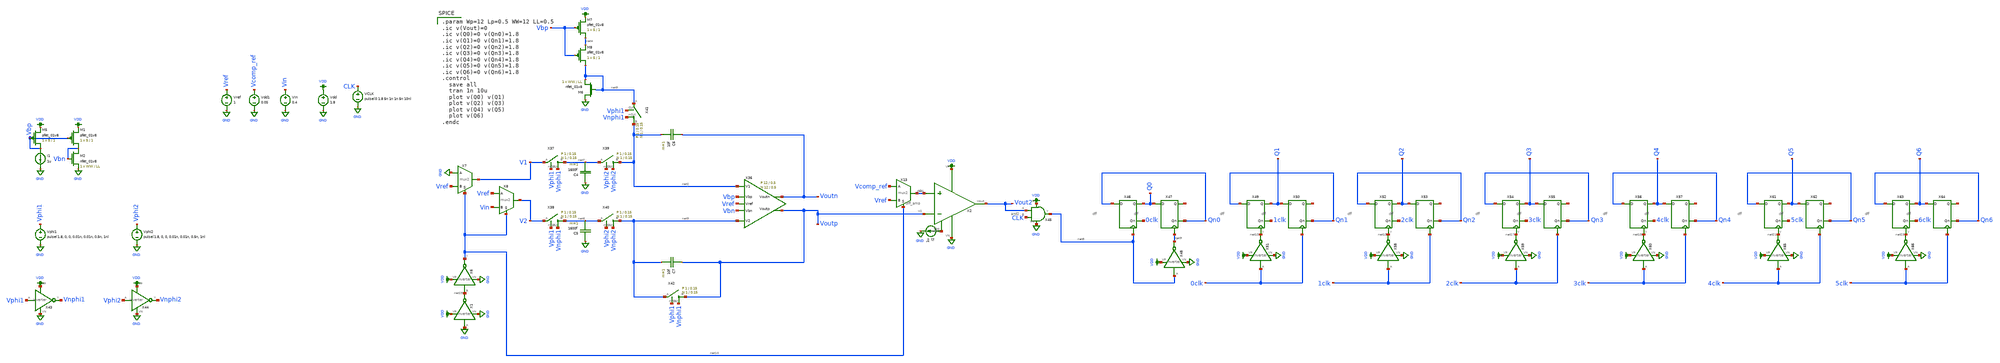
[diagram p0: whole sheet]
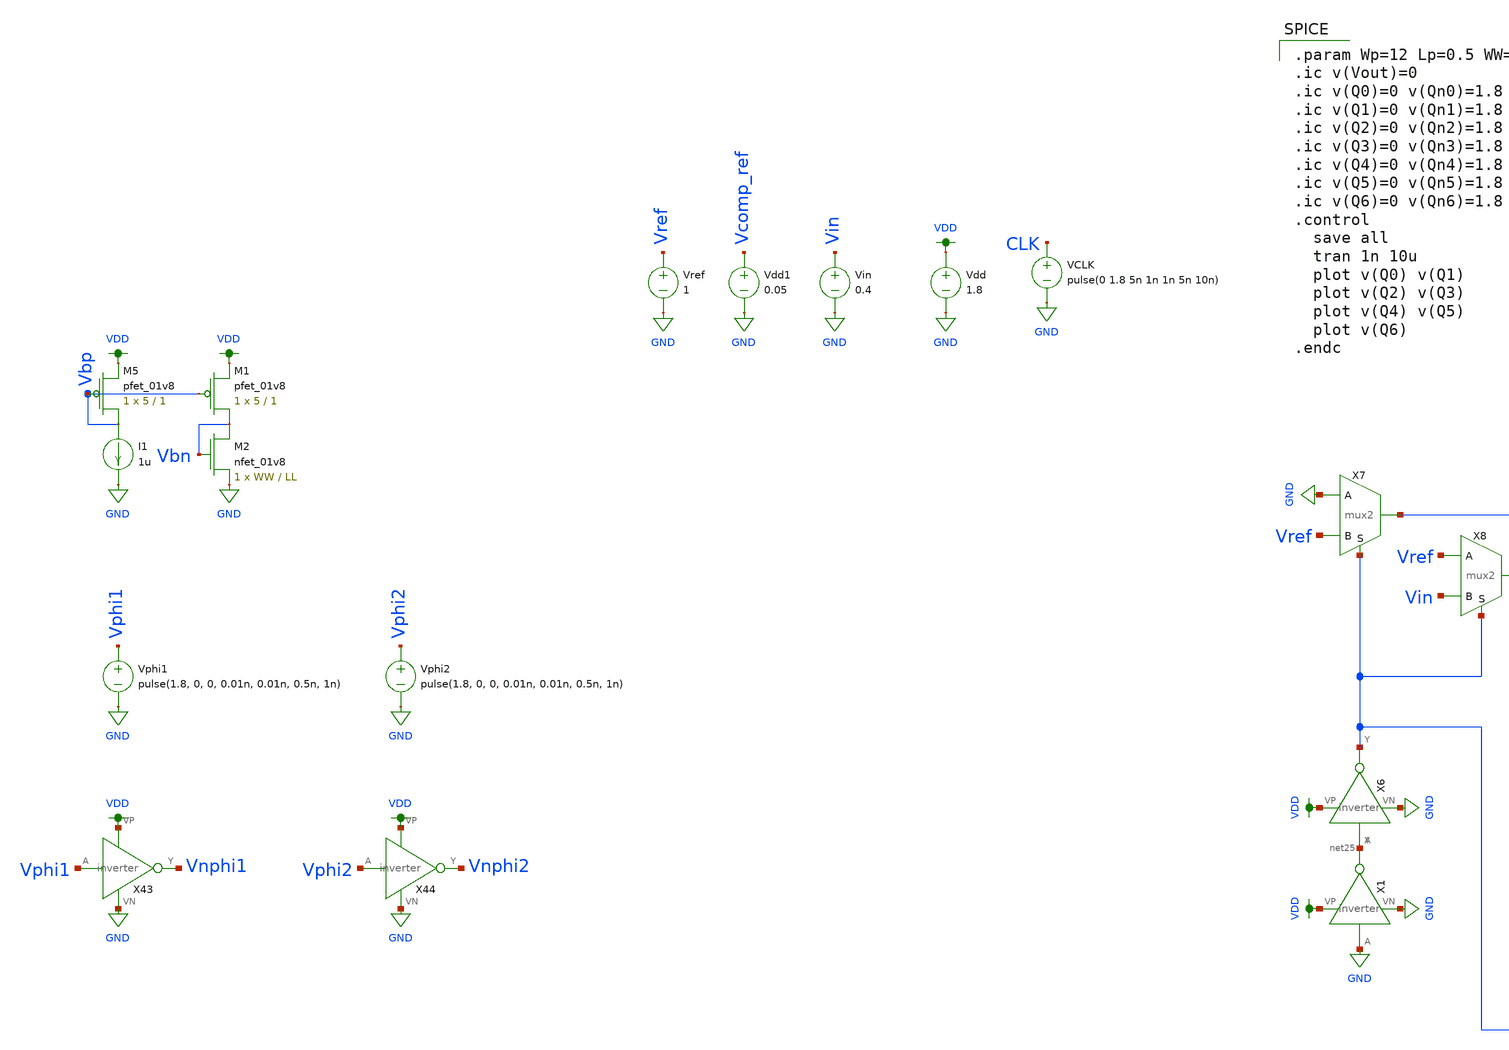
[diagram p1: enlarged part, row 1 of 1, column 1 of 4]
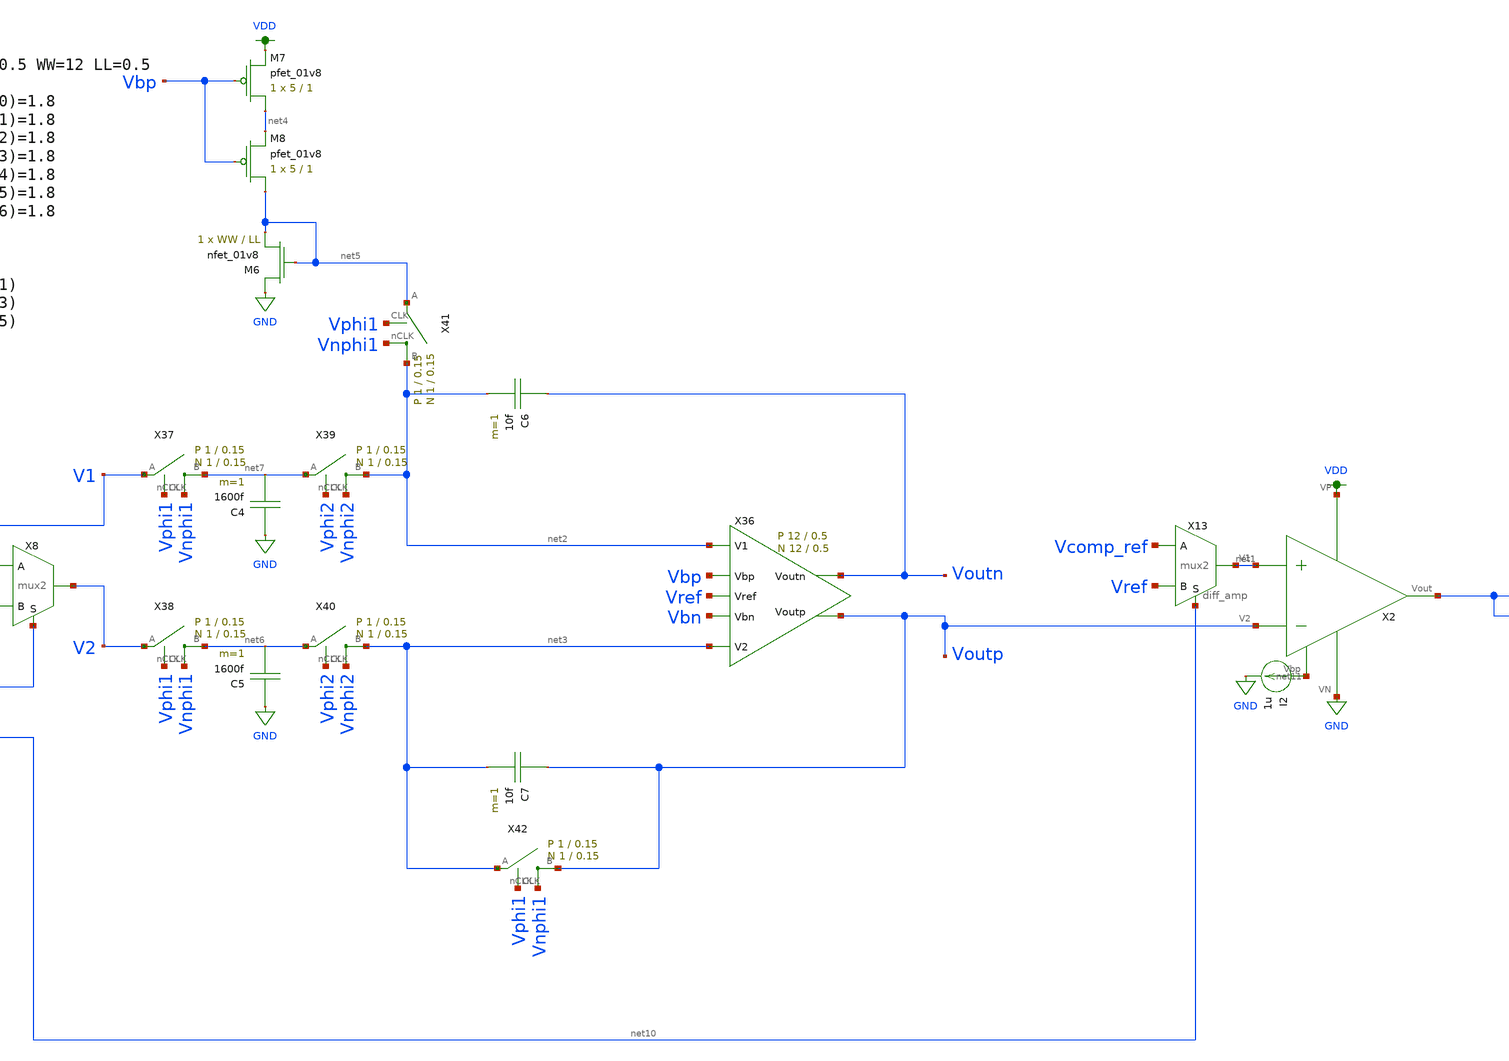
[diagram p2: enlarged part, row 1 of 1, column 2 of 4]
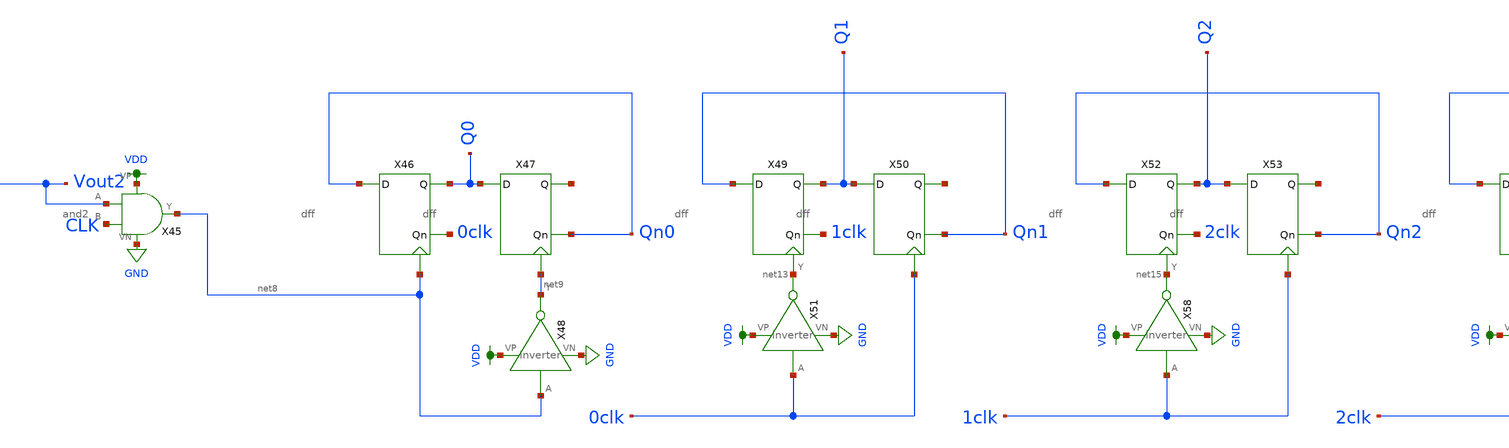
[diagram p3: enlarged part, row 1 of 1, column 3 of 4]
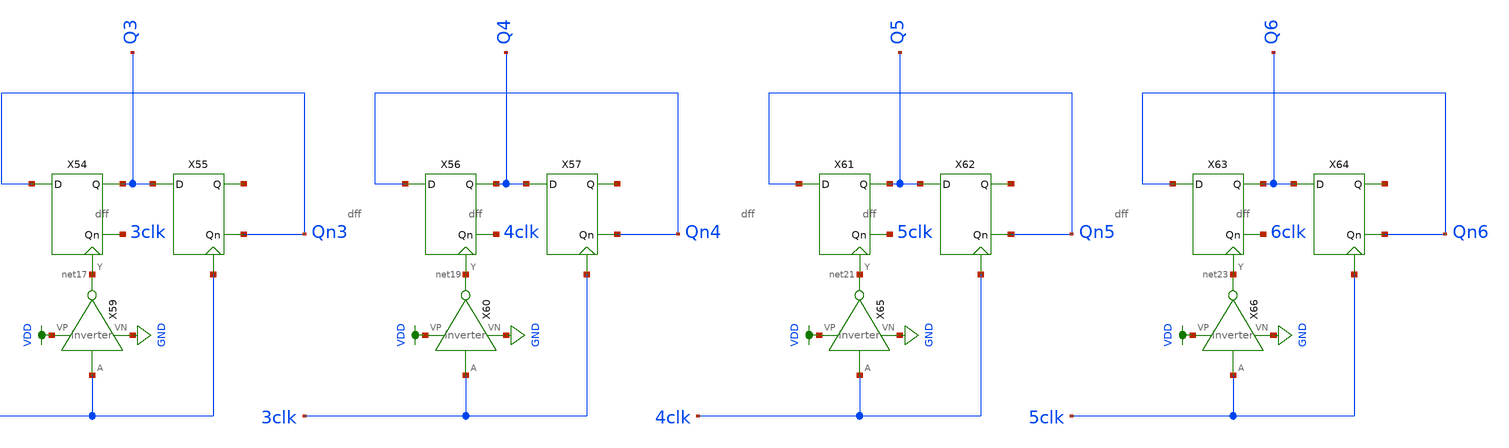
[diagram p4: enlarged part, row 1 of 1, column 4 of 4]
** sch_path: schematic/archive/fg-dual_slope.sch
**.subckt fg-dual_slope
X2 VDD net11 Vout2 net1 Voutp GND diff_amp
Vdd VDD GND 1.8
VCLK CLK GND pulse(0 1.8 5n 1n 1n 5n 10n)
Vdd1 Vcomp_ref GND 0.05
Vin Vin GND 0.4
I2 net11 GND 1u
Vref Vref GND 1
X13 net1 Vcomp_ref Vref net10 mux2
X36 net2 net3 Voutp Voutn Vbp Vref Vbn fully_differential_sc_amp Wp=12 Lp=0.5 WW=12 LL=0.5
C5 GND net6 1600f m=1
C6 Voutn net2 10f m=1
C7 Voutp net3 10f m=1
X38 net6 V2 Vphi1 Vnphi1 switch Wp=1 Lp=0.15 WW=1 LL=0.15
X40 net3 net6 Vphi2 Vnphi2 switch Wp=1 Lp=0.15 WW=1 LL=0.15
X41 net2 net5 Vphi1 Vnphi1 switch Wp=1 Lp=0.15 WW=1 LL=0.15
X42 Voutp net3 Vphi1 Vnphi1 switch Wp=1 Lp=0.15 WW=1 LL=0.15
XM7 net4 Vbp VDD VDD sky130_fd_pr__pfet_01v8 L=1 W=5 nf=1 ad='int((nf+1)/2) * W/nf * 0.29' as='int((nf+2)/2) * W/nf * 0.29'
+ pd='2*int((nf+1)/2) * (W/nf + 0.29)' ps='2*int((nf+2)/2) * (W/nf + 0.29)' nrd='0.29 / W' nrs='0.29 / W'
+ sa=0 sb=0 sd=0 mult=1 m=1
XM8 net5 Vbp net4 VDD sky130_fd_pr__pfet_01v8 L=1 W=5 nf=1 ad='int((nf+1)/2) * W/nf * 0.29' as='int((nf+2)/2) * W/nf * 0.29'
+ pd='2*int((nf+1)/2) * (W/nf + 0.29)' ps='2*int((nf+2)/2) * (W/nf + 0.29)' nrd='0.29 / W' nrs='0.29 / W'
+ sa=0 sb=0 sd=0 mult=1 m=1
XM6 GND net5 net5 GND sky130_fd_pr__nfet_01v8 L=LL W=WW nf=1 ad='int((nf+1)/2) * W/nf * 0.29' as='int((nf+2)/2) * W/nf * 0.29'
+ pd='2*int((nf+1)/2) * (W/nf + 0.29)' ps='2*int((nf+2)/2) * (W/nf + 0.29)' nrd='0.29 / W' nrs='0.29 / W'
+ sa=0 sb=0 sd=0 mult=1 m=1
Vphi1 Vphi1 GND pulse(1.8, 0, 0, 0.01n, 0.01n, 0.5n, 1n)
X43 Vphi1 Vnphi1 VDD GND inverter
Vphi2 Vphi2 GND pulse(1.8, 0, 0, 0.01n, 0.01n, 0.5n, 1n)
X44 Vphi2 Vnphi2 VDD GND inverter
XM5 Vbp Vbp VDD VDD sky130_fd_pr__pfet_01v8 L=1 W=5 nf=1 ad='int((nf+1)/2) * W/nf * 0.29' as='int((nf+2)/2) * W/nf * 0.29'
+ pd='2*int((nf+1)/2) * (W/nf + 0.29)' ps='2*int((nf+2)/2) * (W/nf + 0.29)' nrd='0.29 / W' nrs='0.29 / W'
+ sa=0 sb=0 sd=0 mult=1 m=1
I1 Vbp GND 1u
XM1 Vbn Vbp VDD VDD sky130_fd_pr__pfet_01v8 L=1 W=5 nf=1 ad='int((nf+1)/2) * W/nf * 0.29' as='int((nf+2)/2) * W/nf * 0.29'
+ pd='2*int((nf+1)/2) * (W/nf + 0.29)' ps='2*int((nf+2)/2) * (W/nf + 0.29)' nrd='0.29 / W' nrs='0.29 / W'
+ sa=0 sb=0 sd=0 mult=1 m=1
XM2 Vbn Vbn GND GND sky130_fd_pr__nfet_01v8 L=LL W=WW nf=1 ad='int((nf+1)/2) * W/nf * 0.29' as='int((nf+2)/2) * W/nf * 0.29'
+ pd='2*int((nf+1)/2) * (W/nf + 0.29)' ps='2*int((nf+2)/2) * (W/nf + 0.29)' nrd='0.29 / W' nrs='0.29 / W'
+ sa=0 sb=0 sd=0 mult=1 m=1
C4 GND net7 1600f m=1
X37 net7 V1 Vphi1 Vnphi1 switch Wp=1 Lp=0.15 WW=1 LL=0.15
X39 net2 net7 Vphi2 Vnphi2 switch Wp=1 Lp=0.15 WW=1 LL=0.15
X45 VDD Vout2 GND net8 CLK and2
X46 Qn0 0clk Q0 net8 dff
X47 Q0 Qn0 net12 net9 dff
X48 net8 net9 VDD GND inverter
X49 Qn1 1clk Q1 net13 dff
X50 Q1 Qn1 net14 0clk dff
X51 0clk net13 VDD GND inverter
X52 Qn2 2clk Q2 net15 dff
X53 Q2 Qn2 net16 1clk dff
X54 Qn3 3clk Q3 net17 dff
X55 Q3 Qn3 net18 2clk dff
X56 Qn4 4clk Q4 net19 dff
X57 Q4 Qn4 net20 3clk dff
X58 1clk net15 VDD GND inverter
X59 2clk net17 VDD GND inverter
X60 3clk net19 VDD GND inverter
X61 Qn5 5clk Q5 net21 dff
X62 Q5 Qn5 net22 4clk dff
X63 Qn6 6clk Q6 net23 dff
X64 Q6 Qn6 net24 5clk dff
X65 4clk net21 VDD GND inverter
X66 5clk net23 VDD GND inverter
X1 GND net25 VDD GND inverter
X6 net25 net10 VDD GND inverter
X7 V1 GND Vref net10 mux2
X8 V2 Vref Vin net10 mux2
**** begin user architecture code

.param Wp=12 Lp=0.5 WW=12 LL=0.5
.ic v(Vout)=0
.ic v(Q0)=0 v(Qn0)=1.8
.ic v(Q1)=0 v(Qn1)=1.8
.ic v(Q2)=0 v(Qn2)=1.8
.ic v(Q3)=0 v(Qn3)=1.8
.ic v(Q4)=0 v(Qn4)=1.8
.ic v(Q5)=0 v(Qn5)=1.8
.ic v(Q6)=0 v(Qn6)=1.8
.control
  save all
  tran 1n 10u
  plot v(Q0) v(Q1)
  plot v(Q2) v(Q3)
  plot v(Q4) v(Q5)
  plot v(Q6)
.endc


.option wnflag=1
.param MC_SWITCH=0.0
.lib ~/skywater/skywater-pdk/libraries/sky130_fd_pr_ngspice/latest/models/sky130.lib.spice tt

**** end user architecture code
**.ends
.GLOBAL GND
.GLOBAL VDD
.end
